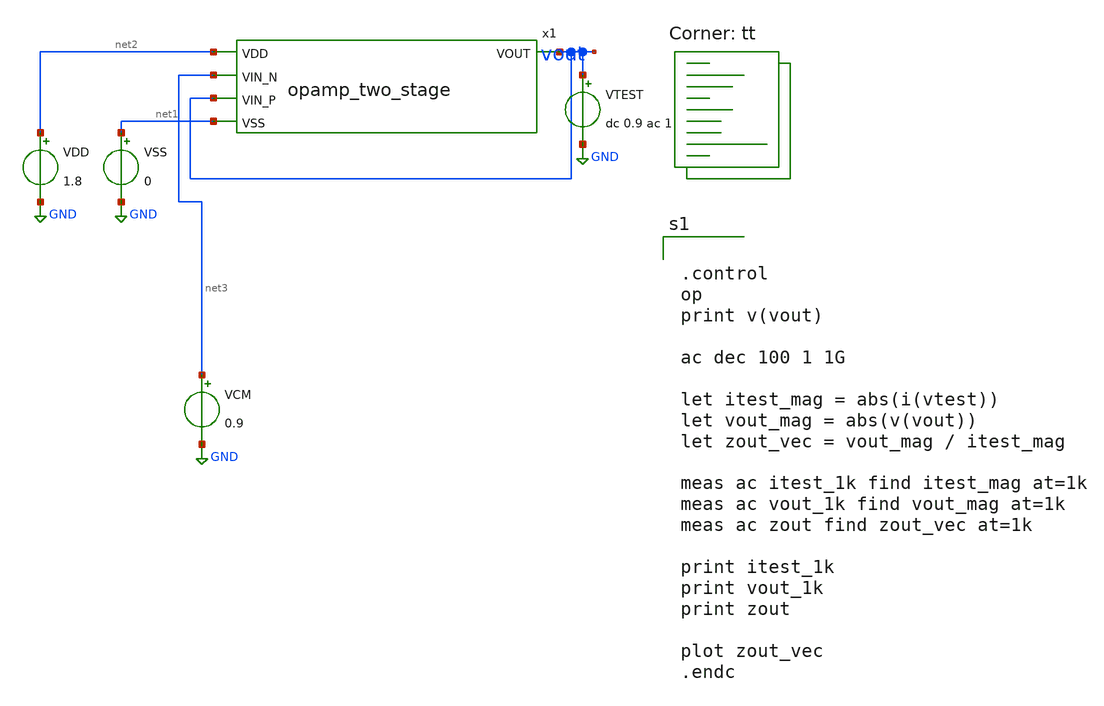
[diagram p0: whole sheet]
** sch_path: analog/build/schematic/tb_output_impedance.sch
**.subckt tb_output_impedance
VSS net1 GND 0
VDD net2 GND 1.8
VCM net3 GND 0.9
VTEST vout GND dc 0.9 ac 1
x1 net2 vout net3 vout net1 opamp_two_stage
**** begin user architecture code
.lib $::SKYWATER_MODELS/sky130.lib.spice tt


.control
op
print v(vout)

ac dec 100 1 1G

let itest_mag = abs(i(vtest))
let vout_mag = abs(v(vout))
let zout_vec = vout_mag / itest_mag

meas ac itest_1k find itest_mag at=1k
meas ac vout_1k find vout_mag at=1k
meas ac zout find zout_vec at=1k

print itest_1k
print vout_1k
print zout

plot zout_vec
.endc


**** end user architecture code
**.ends

* expanding   symbol:  opamp_two_stage.sym # of pins=5
** sym_path: analog/build/schematic/opamp_two_stage.sym
** sch_path: analog/build/schematic/opamp_two_stage.sch
.subckt opamp_two_stage VDD VOUT VIN_N VIN_P VSS
*.ipin VIN_N
*.ipin VIN_P
*.opin VOUT
*.ipin VDD
*.ipin VSS
XM1 net3 VIN_N net1 VSS sky130_fd_pr__nfet_01v8 L=1 W=10 nf=1 ad='int((nf+1)/2) * W/nf * 0.29' as='int((nf+2)/2) * W/nf * 0.29'
+ pd='2*int((nf+1)/2) * (W/nf + 0.29)' ps='2*int((nf+2)/2) * (W/nf + 0.29)' nrd='0.29 / W' nrs='0.29 / W'
+ sa=0 sb=0 sd=0 mult=1 m=1
XM2 net2 VIN_P net1 VSS sky130_fd_pr__nfet_01v8 L=1 W=10 nf=1 ad='int((nf+1)/2) * W/nf * 0.29' as='int((nf+2)/2) * W/nf * 0.29'
+ pd='2*int((nf+1)/2) * (W/nf + 0.29)' ps='2*int((nf+2)/2) * (W/nf + 0.29)' nrd='0.29 / W' nrs='0.29 / W'
+ sa=0 sb=0 sd=0 mult=1 m=1
XM3 net1 net5 VSS VSS sky130_fd_pr__nfet_01v8 L=2 W=10 nf=1 ad='int((nf+1)/2) * W/nf * 0.29' as='int((nf+2)/2) * W/nf * 0.29'
+ pd='2*int((nf+1)/2) * (W/nf + 0.29)' ps='2*int((nf+2)/2) * (W/nf + 0.29)' nrd='0.29 / W' nrs='0.29 / W'
+ sa=0 sb=0 sd=0 mult=1 m=1
XM4 net3 net2 VDD VDD sky130_fd_pr__pfet_01v8 L=1 W=20 nf=1 ad='int((nf+1)/2) * W/nf * 0.29' as='int((nf+2)/2) * W/nf * 0.29'
+ pd='2*int((nf+1)/2) * (W/nf + 0.29)' ps='2*int((nf+2)/2) * (W/nf + 0.29)' nrd='0.29 / W' nrs='0.29 / W'
+ sa=0 sb=0 sd=0 mult=1 m=1
XM5 net2 net2 VDD VDD sky130_fd_pr__pfet_01v8 L=1 W=20 nf=1 ad='int((nf+1)/2) * W/nf * 0.29' as='int((nf+2)/2) * W/nf * 0.29'
+ pd='2*int((nf+1)/2) * (W/nf + 0.29)' ps='2*int((nf+2)/2) * (W/nf + 0.29)' nrd='0.29 / W' nrs='0.29 / W'
+ sa=0 sb=0 sd=0 mult=1 m=1
XM7 VOUT net5 VSS VSS sky130_fd_pr__nfet_01v8 L=2 W=10 nf=1 ad='int((nf+1)/2) * W/nf * 0.29' as='int((nf+2)/2) * W/nf * 0.29'
+ pd='2*int((nf+1)/2) * (W/nf + 0.29)' ps='2*int((nf+2)/2) * (W/nf + 0.29)' nrd='0.29 / W' nrs='0.29 / W'
+ sa=0 sb=0 sd=0 mult=1 m=1
XM8 VOUT net3 VDD VDD sky130_fd_pr__pfet_01v8 L=1 W=20 nf=1 ad='int((nf+1)/2) * W/nf * 0.29' as='int((nf+2)/2) * W/nf * 0.29'
+ pd='2*int((nf+1)/2) * (W/nf + 0.29)' ps='2*int((nf+2)/2) * (W/nf + 0.29)' nrd='0.29 / W' nrs='0.29 / W'
+ sa=0 sb=0 sd=0 mult=1 m=1
C1 net3 net4 1p m=1
R1 VOUT net4 2k m=1
XM_bias net5 net5 VSS VSS sky130_fd_pr__nfet_01v8 L=2 W=10 nf=1 ad='int((nf+1)/2) * W/nf * 0.29' as='int((nf+2)/2) * W/nf * 0.29'
+ pd='2*int((nf+1)/2) * (W/nf + 0.29)' ps='2*int((nf+2)/2) * (W/nf + 0.29)' nrd='0.29 / W' nrs='0.29 / W'
+ sa=0 sb=0 sd=0 mult=1 m=1
R2 VDD net5 10k m=1
.ends

.GLOBAL GND
.end
